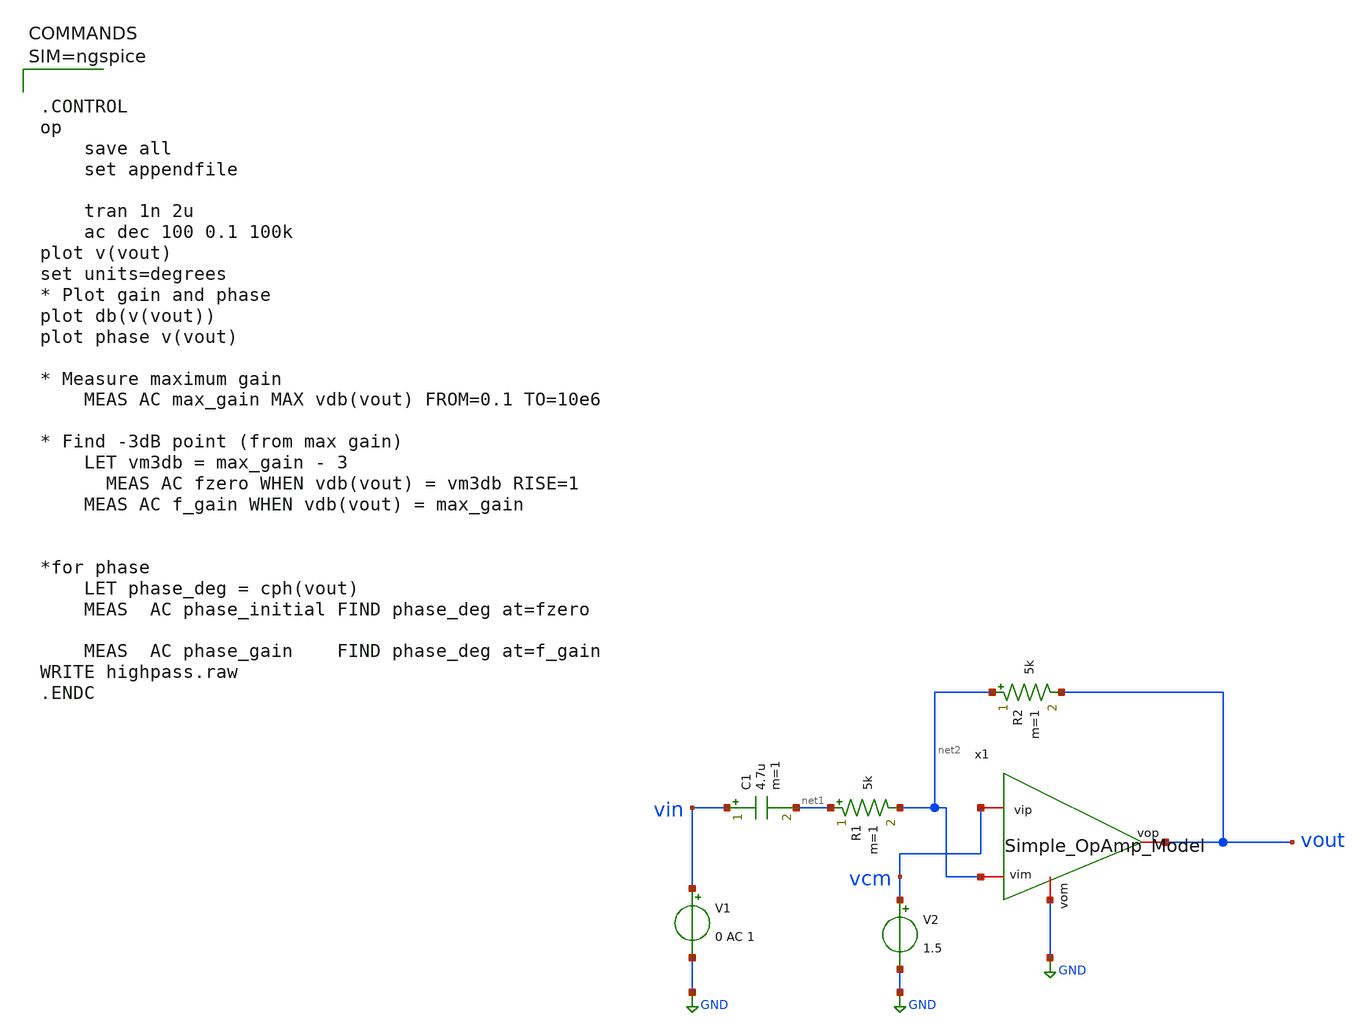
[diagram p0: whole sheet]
** sch_path: work/xschem/highpass.sch
**.subckt highpass
x1 vout vcm net2 GND Simple_OpAmp_Model
V1 vin GND 0 AC 1
R1 net1 net2 5k m=1
C1 vin net1 4.7u m=1
V2 vcm GND 1.5
R2 net2 vout 5k m=1
**** begin user architecture code



.CONTROL
op
	save all
	set appendfile

	tran 1n 2u
	ac dec 100 0.1 100k
plot v(vout)
set units=degrees
* Plot gain and phase
plot db(v(vout))
plot phase v(vout)

* Measure maximum gain
	MEAS AC max_gain MAX vdb(vout) FROM=0.1 TO=10e6

* Find -3dB point (from max gain)
	LET vm3db = max_gain - 3
  	MEAS AC fzero WHEN vdb(vout) = vm3db RISE=1
	MEAS AC f_gain WHEN vdb(vout) = max_gain


*for phase
	LET phase_deg = cph(vout)
	MEAS  AC phase_initial FIND phase_deg at=fzero

	MEAS  AC phase_gain    FIND phase_deg at=f_gain
WRITE highpass.raw
.ENDC



**** end user architecture code
**.ends

* expanding   symbol:  Simple_OpAmp_Model.sym # of pins=4
** sym_path: work/xschem/Simple_OpAmp_Model.sym
** sch_path: work/xschem/Simple_OpAmp_Model.sch
.subckt Simple_OpAmp_Model vop vip vim vom
*.iopin vop
*.iopin vom
*.iopin vim
*.iopin vip
E1 vop vom vip vim 1000
.ends

.GLOBAL GND
.end
